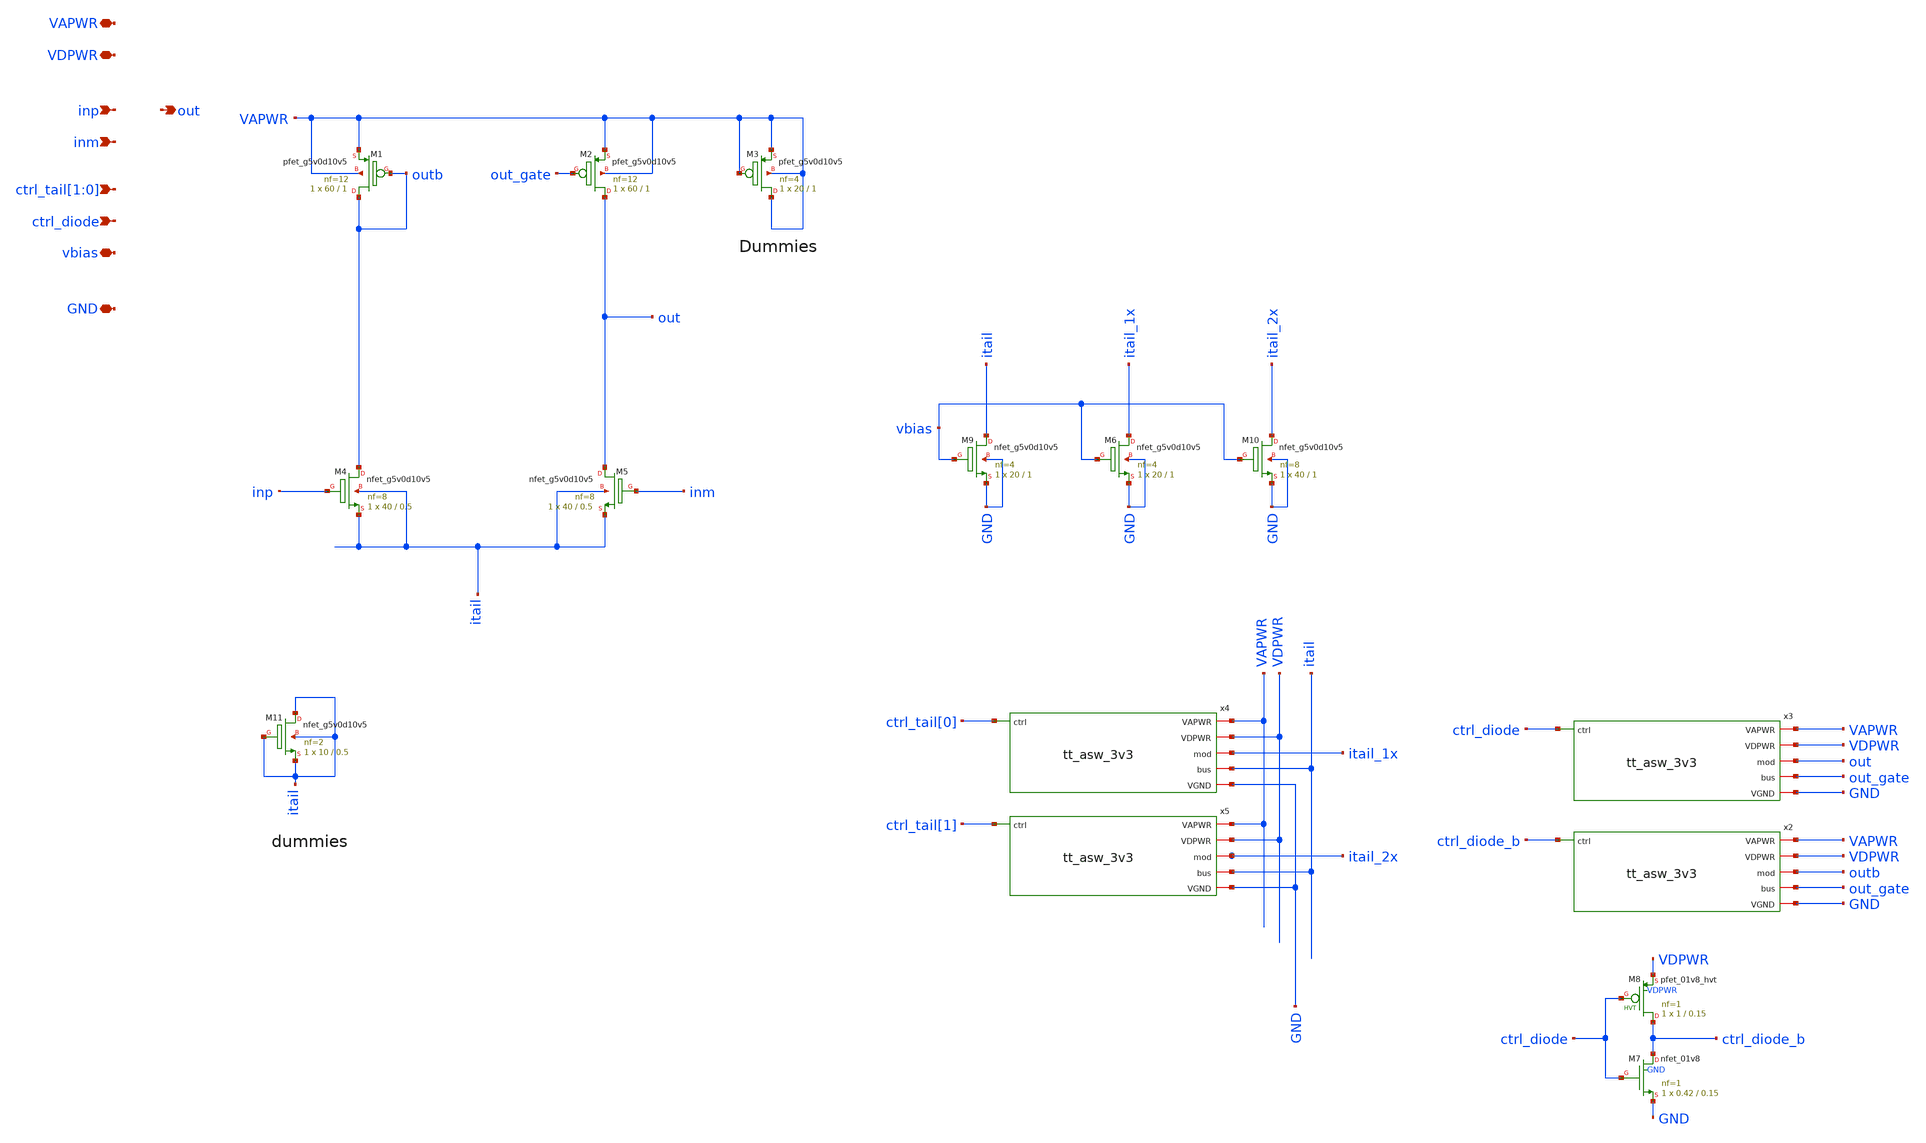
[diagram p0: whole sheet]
** sch_path: tt_um_mosbius/xschem/ota_n.sch
**.subckt ota_n vbias ctrl_tail[1],ctrl_tail[0] VAPWR VDPWR GND ctrl_diode inp inm out
*.iopin vbias
*.ipin ctrl_tail[1],ctrl_tail[0]
*.iopin VAPWR
*.iopin VDPWR
*.iopin GND
*.ipin ctrl_diode
*.ipin inp
*.ipin inm
*.opin out
XM1 outb outb VAPWR VAPWR sky130_fd_pr__pfet_g5v0d10v5 L=1 W=60 nf=12 ad='int((nf+1)/2) * W/nf * 0.29'
+ as='int((nf+2)/2) * W/nf * 0.29' pd='2*int((nf+1)/2) * (W/nf + 0.29)' ps='2*int((nf+2)/2) * (W/nf + 0.29)'
+ nrd='0.29 / W' nrs='0.29 / W' sa=0 sb=0 sd=0 mult=1 m=1
XM2 out out_gate VAPWR VAPWR sky130_fd_pr__pfet_g5v0d10v5 L=1 W=60 nf=12 ad='int((nf+1)/2) * W/nf * 0.29'
+ as='int((nf+2)/2) * W/nf * 0.29' pd='2*int((nf+1)/2) * (W/nf + 0.29)' ps='2*int((nf+2)/2) * (W/nf + 0.29)'
+ nrd='0.29 / W' nrs='0.29 / W' sa=0 sb=0 sd=0 mult=1 m=1
x2 GND VDPWR VAPWR ctrl_diode_b outb out_gate tt_asw_3v3
x3 GND VDPWR VAPWR ctrl_diode out out_gate tt_asw_3v3
XM7 ctrl_diode_b ctrl_diode GND GND sky130_fd_pr__nfet_01v8 L=0.15 W=0.42 nf=1 ad='int((nf+1)/2) * W/nf * 0.29'
+ as='int((nf+2)/2) * W/nf * 0.29' pd='2*int((nf+1)/2) * (W/nf + 0.29)' ps='2*int((nf+2)/2) * (W/nf + 0.29)'
+ nrd='0.29 / W' nrs='0.29 / W' sa=0 sb=0 sd=0 mult=1 m=1
XM8 ctrl_diode_b ctrl_diode VDPWR VDPWR sky130_fd_pr__pfet_01v8_hvt L=0.15 W=1 nf=1 ad='int((nf+1)/2) * W/nf * 0.29'
+ as='int((nf+2)/2) * W/nf * 0.29' pd='2*int((nf+1)/2) * (W/nf + 0.29)' ps='2*int((nf+2)/2) * (W/nf + 0.29)'
+ nrd='0.29 / W' nrs='0.29 / W' sa=0 sb=0 sd=0 mult=1 m=1
XM3 VAPWR VAPWR VAPWR VAPWR sky130_fd_pr__pfet_g5v0d10v5 L=1 W=20 nf=4 ad='int((nf+1)/2) * W/nf * 0.29'
+ as='int((nf+2)/2) * W/nf * 0.29' pd='2*int((nf+1)/2) * (W/nf + 0.29)' ps='2*int((nf+2)/2) * (W/nf + 0.29)'
+ nrd='0.29 / W' nrs='0.29 / W' sa=0 sb=0 sd=0 mult=1 m=1
XM4 outb inp itail itail sky130_fd_pr__nfet_g5v0d10v5 L=0.5 W=40 nf=8 ad='int((nf+1)/2) * W/nf * 0.29'
+ as='int((nf+2)/2) * W/nf * 0.29' pd='2*int((nf+1)/2) * (W/nf + 0.29)' ps='2*int((nf+2)/2) * (W/nf + 0.29)'
+ nrd='0.29 / W' nrs='0.29 / W' sa=0 sb=0 sd=0 mult=1 m=1
XM5 out inm itail itail sky130_fd_pr__nfet_g5v0d10v5 L=0.5 W=40 nf=8 ad='int((nf+1)/2) * W/nf * 0.29'
+ as='int((nf+2)/2) * W/nf * 0.29' pd='2*int((nf+1)/2) * (W/nf + 0.29)' ps='2*int((nf+2)/2) * (W/nf + 0.29)'
+ nrd='0.29 / W' nrs='0.29 / W' sa=0 sb=0 sd=0 mult=1 m=1
XM6 itail_1x vbias GND GND sky130_fd_pr__nfet_g5v0d10v5 L=1 W=20 nf=4 ad='int((nf+1)/2) * W/nf * 0.29'
+ as='int((nf+2)/2) * W/nf * 0.29' pd='2*int((nf+1)/2) * (W/nf + 0.29)' ps='2*int((nf+2)/2) * (W/nf + 0.29)'
+ nrd='0.29 / W' nrs='0.29 / W' sa=0 sb=0 sd=0 mult=1 m=1
XM9 itail vbias GND GND sky130_fd_pr__nfet_g5v0d10v5 L=1 W=20 nf=4 ad='int((nf+1)/2) * W/nf * 0.29' as='int((nf+2)/2) * W/nf * 0.29'
+ pd='2*int((nf+1)/2) * (W/nf + 0.29)' ps='2*int((nf+2)/2) * (W/nf + 0.29)' nrd='0.29 / W' nrs='0.29 / W'
+ sa=0 sb=0 sd=0 mult=1 m=1
XM10 itail_2x vbias GND GND sky130_fd_pr__nfet_g5v0d10v5 L=1 W=40 nf=8 ad='int((nf+1)/2) * W/nf * 0.29'
+ as='int((nf+2)/2) * W/nf * 0.29' pd='2*int((nf+1)/2) * (W/nf + 0.29)' ps='2*int((nf+2)/2) * (W/nf + 0.29)'
+ nrd='0.29 / W' nrs='0.29 / W' sa=0 sb=0 sd=0 mult=1 m=1
x4 GND VDPWR VAPWR ctrl_tail[0] itail_1x itail tt_asw_3v3
x5 GND VDPWR VAPWR ctrl_tail[1] itail_2x itail tt_asw_3v3
XM11 itail itail itail itail sky130_fd_pr__nfet_g5v0d10v5 L=0.5 W=10 nf=2 ad='int((nf+1)/2) * W/nf * 0.29'
+ as='int((nf+2)/2) * W/nf * 0.29' pd='2*int((nf+1)/2) * (W/nf + 0.29)' ps='2*int((nf+2)/2) * (W/nf + 0.29)'
+ nrd='0.29 / W' nrs='0.29 / W' sa=0 sb=0 sd=0 mult=1 m=1
**.ends

* expanding   symbol:  tt_asw_3v3.sym # of pins=6
** sym_path: tt_asw_3v3.sym
** sch_path: tt_asw_3v3.sch
.subckt tt_asw_3v3 VGND VDPWR VAPWR ctrl mod bus
*.iopin mod
*.iopin bus
*.ipin ctrl
*.iopin VGND
*.iopin VDPWR
*.iopin VAPWR
XM1 tgon_n net2 VAPWR VAPWR sky130_fd_pr__pfet_g5v0d10v5 L=0.5 W=0.84 nf=1 ad='int((nf+1)/2) * W/nf * 0.29'
+ as='int((nf+2)/2) * W/nf * 0.29' pd='2*int((nf+1)/2) * (W/nf + 0.29)' ps='2*int((nf+2)/2) * (W/nf + 0.29)'
+ nrd='0.29 / W' nrs='0.29 / W' sa=0 sb=0 sd=0 mult=1 m=1
XM2 tgon_n net2 VGND VGND sky130_fd_pr__nfet_g5v0d10v5 L=0.5 W=0.42 nf=1 ad='int((nf+1)/2) * W/nf * 0.29'
+ as='int((nf+2)/2) * W/nf * 0.29' pd='2*int((nf+1)/2) * (W/nf + 0.29)' ps='2*int((nf+2)/2) * (W/nf + 0.29)'
+ nrd='0.29 / W' nrs='0.29 / W' sa=0 sb=0 sd=0 mult=1 m=1
XM3 tgon net1 VAPWR VAPWR sky130_fd_pr__pfet_g5v0d10v5 L=0.5 W=0.84 nf=1 ad='int((nf+1)/2) * W/nf * 0.29'
+ as='int((nf+2)/2) * W/nf * 0.29' pd='2*int((nf+1)/2) * (W/nf + 0.29)' ps='2*int((nf+2)/2) * (W/nf + 0.29)'
+ nrd='0.29 / W' nrs='0.29 / W' sa=0 sb=0 sd=0 mult=1 m=1
XM4 tgon net1 VGND VGND sky130_fd_pr__nfet_g5v0d10v5 L=0.5 W=0.42 nf=1 ad='int((nf+1)/2) * W/nf * 0.29'
+ as='int((nf+2)/2) * W/nf * 0.29' pd='2*int((nf+1)/2) * (W/nf + 0.29)' ps='2*int((nf+2)/2) * (W/nf + 0.29)'
+ nrd='0.29 / W' nrs='0.29 / W' sa=0 sb=0 sd=0 mult=1 m=1
XM5 bus tgon_n mod VAPWR sky130_fd_pr__pfet_g5v0d10v5 L=0.5 W=180 nf=18 ad='int((nf+1)/2) * W/nf * 0.29'
+ as='int((nf+2)/2) * W/nf * 0.29' pd='2*int((nf+1)/2) * (W/nf + 0.29)' ps='2*int((nf+2)/2) * (W/nf + 0.29)'
+ nrd='0.29 / W' nrs='0.29 / W' sa=0 sb=0 sd=0 mult=1 m=1
XM6 bus tgon mod VGND sky130_fd_pr__nfet_g5v0d10v5 L=0.5 W=60 nf=12 ad='int((nf+1)/2) * W/nf * 0.29'
+ as='int((nf+2)/2) * W/nf * 0.29' pd='2*int((nf+1)/2) * (W/nf + 0.29)' ps='2*int((nf+2)/2) * (W/nf + 0.29)'
+ nrd='0.29 / W' nrs='0.29 / W' sa=0 sb=0 sd=0 mult=1 m=1
XM7 ctrl_n ctrl VGND VGND sky130_fd_pr__nfet_01v8 L=0.15 W=0.42 nf=1 ad='int((nf+1)/2) * W/nf * 0.29'
+ as='int((nf+2)/2) * W/nf * 0.29' pd='2*int((nf+1)/2) * (W/nf + 0.29)' ps='2*int((nf+2)/2) * (W/nf + 0.29)'
+ nrd='0.29 / W' nrs='0.29 / W' sa=0 sb=0 sd=0 mult=1 m=1
XM8 ctrl_n ctrl VDPWR VDPWR sky130_fd_pr__pfet_01v8_hvt L=0.15 W=1 nf=1 ad='int((nf+1)/2) * W/nf * 0.29'
+ as='int((nf+2)/2) * W/nf * 0.29' pd='2*int((nf+1)/2) * (W/nf + 0.29)' ps='2*int((nf+2)/2) * (W/nf + 0.29)'
+ nrd='0.29 / W' nrs='0.29 / W' sa=0 sb=0 sd=0 mult=1 m=1
XM9 net1 ctrl VGND VGND sky130_fd_pr__nfet_g5v0d10v5 L=0.5 W=0.42 nf=1 ad='int((nf+1)/2) * W/nf * 0.29'
+ as='int((nf+2)/2) * W/nf * 0.29' pd='2*int((nf+1)/2) * (W/nf + 0.29)' ps='2*int((nf+2)/2) * (W/nf + 0.29)'
+ nrd='0.29 / W' nrs='0.29 / W' sa=0 sb=0 sd=0 mult=1 m=1
XM10 net2 ctrl_n VGND VGND sky130_fd_pr__nfet_g5v0d10v5 L=0.5 W=0.42 nf=1 ad='int((nf+1)/2) * W/nf * 0.29'
+ as='int((nf+2)/2) * W/nf * 0.29' pd='2*int((nf+1)/2) * (W/nf + 0.29)' ps='2*int((nf+2)/2) * (W/nf + 0.29)'
+ nrd='0.29 / W' nrs='0.29 / W' sa=0 sb=0 sd=0 mult=1 m=1
XM11 net1 net2 net3 VAPWR sky130_fd_pr__pfet_g5v0d10v5 L=0.5 W=0.42 nf=1 ad='int((nf+1)/2) * W/nf * 0.29'
+ as='int((nf+2)/2) * W/nf * 0.29' pd='2*int((nf+1)/2) * (W/nf + 0.29)' ps='2*int((nf+2)/2) * (W/nf + 0.29)'
+ nrd='0.29 / W' nrs='0.29 / W' sa=0 sb=0 sd=0 mult=1 m=1
XM12 net2 net1 net4 VAPWR sky130_fd_pr__pfet_g5v0d10v5 L=0.5 W=0.42 nf=1 ad='int((nf+1)/2) * W/nf * 0.29'
+ as='int((nf+2)/2) * W/nf * 0.29' pd='2*int((nf+1)/2) * (W/nf + 0.29)' ps='2*int((nf+2)/2) * (W/nf + 0.29)'
+ nrd='0.29 / W' nrs='0.29 / W' sa=0 sb=0 sd=0 mult=1 m=1
XM13 net3 net1 VAPWR VAPWR sky130_fd_pr__pfet_g5v0d10v5 L=0.5 W=0.42 nf=1 ad='int((nf+1)/2) * W/nf * 0.29'
+ as='int((nf+2)/2) * W/nf * 0.29' pd='2*int((nf+1)/2) * (W/nf + 0.29)' ps='2*int((nf+2)/2) * (W/nf + 0.29)'
+ nrd='0.29 / W' nrs='0.29 / W' sa=0 sb=0 sd=0 mult=1 m=1
XM14 net4 net2 VAPWR VAPWR sky130_fd_pr__pfet_g5v0d10v5 L=0.5 W=0.42 nf=1 ad='int((nf+1)/2) * W/nf * 0.29'
+ as='int((nf+2)/2) * W/nf * 0.29' pd='2*int((nf+1)/2) * (W/nf + 0.29)' ps='2*int((nf+2)/2) * (W/nf + 0.29)'
+ nrd='0.29 / W' nrs='0.29 / W' sa=0 sb=0 sd=0 mult=1 m=1
.ends

.end
